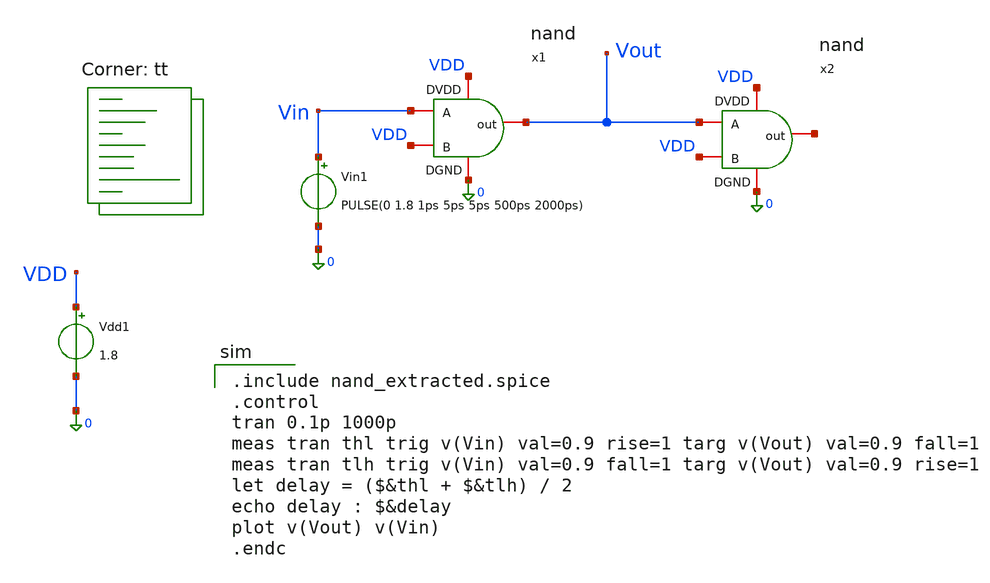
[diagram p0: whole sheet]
** sch_path: tutorial-5/source/qn_1_a.sch
**.subckt qn_1_a
x1 VDD 0 Vin VDD Vout nand
x2 VDD 0 Vout VDD net1 nand
Vin1 Vin 0 PULSE(0 1.8 1ps 5ps 5ps 500ps 2000ps)
Vdd1 VDD 0 1.8
**** begin user architecture code

.include nand_extracted.spice
.control
tran 0.1p 1000p
meas tran thl trig v(Vin) val=0.9 rise=1 targ v(Vout) val=0.9 fall=1
meas tran tlh trig v(Vin) val=0.9 fall=1 targ v(Vout) val=0.9 rise=1
let delay = ($&thl + $&tlh) / 2
echo delay : $&delay
plot v(Vout) v(Vin)
.endc

.lib $::SKYWATER_MODELS/sky130.lib.spice tt
**** end user architecture code
**.ends

* expanding   symbol:  nand.sym # of pins=5
** sym_path: tutorial-5/source/nand.sym
** sch_path: tutorial-5/source/nand.sch
.subckt nand DVDD DGND A B out
*.iopin DVDD
*.iopin DGND
*.iopin A
*.iopin B
*.iopin out
XM1 DVDD B out DVDD sky130_fd_pr__pfet_01v8 L=0.15 W=1.68 nf=1 ad='int((nf+1)/2) * W/nf * 0.29' as='int((nf+2)/2) * W/nf * 0.29'
+ pd='2*int((nf+1)/2) * (W/nf + 0.29)' ps='2*int((nf+2)/2) * (W/nf + 0.29)' nrd='0.29 / W' nrs='0.29 / W'
+ sa=0 sb=0 sd=0 mult=1 m=1
XM2 out A DVDD DVDD sky130_fd_pr__pfet_01v8 L=0.15 W=1.68 nf=1 ad='int((nf+1)/2) * W/nf * 0.29' as='int((nf+2)/2) * W/nf * 0.29'
+ pd='2*int((nf+1)/2) * (W/nf + 0.29)' ps='2*int((nf+2)/2) * (W/nf + 0.29)' nrd='0.29 / W' nrs='0.29 / W'
+ sa=0 sb=0 sd=0 mult=1 m=1
XM3 out A net1 DGND sky130_fd_pr__nfet_01v8 L=0.15 W=1.68 nf=1 ad='int((nf+1)/2) * W/nf * 0.29' as='int((nf+2)/2) * W/nf * 0.29'
+ pd='2*int((nf+1)/2) * (W/nf + 0.29)' ps='2*int((nf+2)/2) * (W/nf + 0.29)' nrd='0.29 / W' nrs='0.29 / W'
+ sa=0 sb=0 sd=0 mult=1 m=1
XM4 DGND B net1 DGND sky130_fd_pr__nfet_01v8 L=0.15 W=1.68 nf=1 ad='int((nf+1)/2) * W/nf * 0.29' as='int((nf+2)/2) * W/nf * 0.29'
+ pd='2*int((nf+1)/2) * (W/nf + 0.29)' ps='2*int((nf+2)/2) * (W/nf + 0.29)' nrd='0.29 / W' nrs='0.29 / W'
+ sa=0 sb=0 sd=0 mult=1 m=1
.ends

.end
